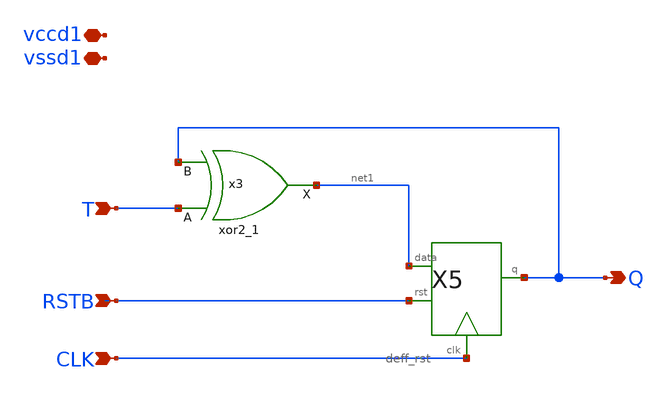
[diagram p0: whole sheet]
** sch_path: xschem/T_flip_flop/asyn_rst_t_dff_vccd.sch
**.subckt asyn_rst_t_dff_vccd T CLK Q RSTB vccd1 vssd1
*.ipin T
*.ipin CLK
*.opin Q
*.ipin RSTB
*.iopin vccd1
*.iopin vssd1
x3 T Q vssd1 vssd1 vccd1 vccd1 net1 sky130_fd_sc_hd__xor2_1
X5 net1 CLK Q RSTB deff_rst
**.ends

* expanding   symbol:  tryandtest/deff_rst.sym # of pins=4
** sym_path: xschem/tryandtest/deff_rst.sym
** sch_path: xschem/tryandtest/deff_rst.sch
.subckt deff_rst data clk q rst
*.ipin clk
*.ipin data
*.opin q
*.ipin rst
x3 net2 net3 clk GND GND VDD VDD q sky130_fd_sc_lp__mux2_1
x21 net1 data rst GND GND VDD VDD net2 sky130_fd_sc_lp__dfrtn_1
x2 net4 GND GND VDD VDD net1 sky130_fd_sc_lp__inv_1
x5 net5 GND GND VDD VDD net4 sky130_fd_sc_lp__inv_1
x1 net1 data rst GND GND VDD VDD net3 sky130_fd_sc_lp__dfrtp_1
x4 net6 GND GND VDD VDD net5 sky130_fd_sc_lp__inv_1
x6 clk GND GND VDD VDD net6 sky130_fd_sc_lp__inv_1
.ends

.end
